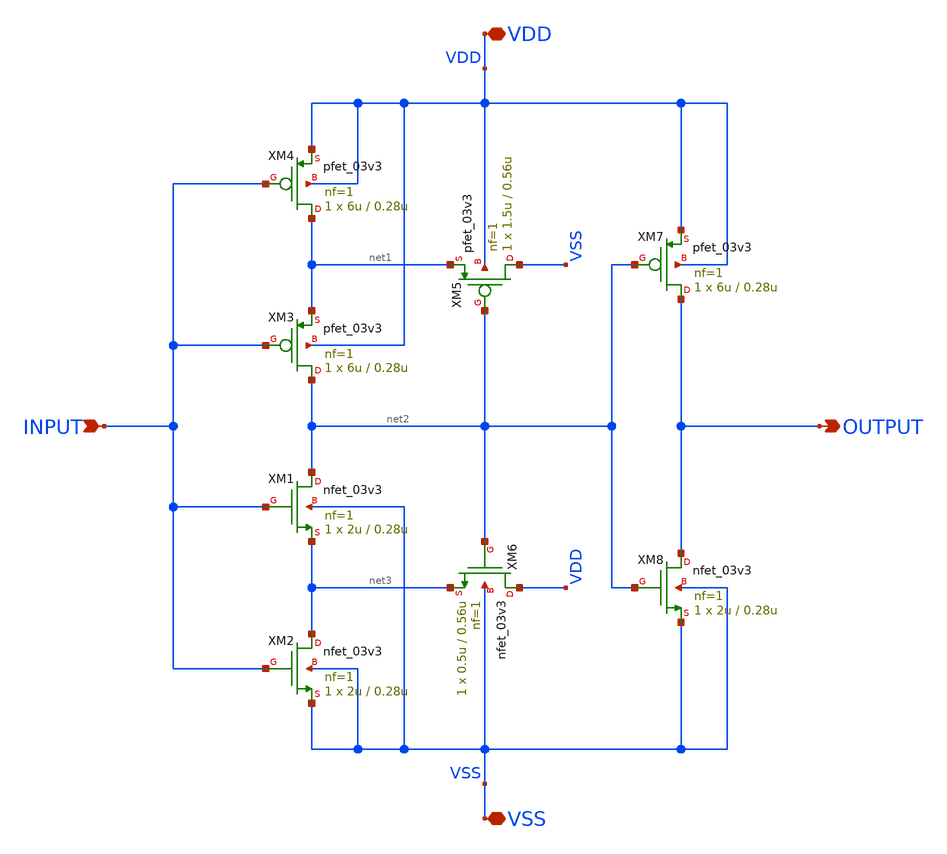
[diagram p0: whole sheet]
** sch_path: designs/schmitt_trigger/schmitt_trigger.sch
**.subckt schmitt_trigger INPUT OUTPUT VSS VDD
*.ipin INPUT
*.opin OUTPUT
*.iopin VSS
*.iopin VDD
XM1 net2 INPUT net3 VSS nfet_03v3 L=0.28u W=2u nf=1 ad='int((nf+1)/2) * W/nf * 0.18u' as='int((nf+2)/2) * W/nf * 0.18u'
+ pd='2*int((nf+1)/2) * (W/nf + 0.18u)' ps='2*int((nf+2)/2) * (W/nf + 0.18u)' nrd='0.18u / W' nrs='0.18u / W'
+ sa=0 sb=0 sd=0 m=1
XM2 net3 INPUT VSS VSS nfet_03v3 L=0.28u W=2u nf=1 ad='int((nf+1)/2) * W/nf * 0.18u' as='int((nf+2)/2) * W/nf * 0.18u'
+ pd='2*int((nf+1)/2) * (W/nf + 0.18u)' ps='2*int((nf+2)/2) * (W/nf + 0.18u)' nrd='0.18u / W' nrs='0.18u / W'
+ sa=0 sb=0 sd=0 m=1
XM3 net2 INPUT net1 VDD pfet_03v3 L=0.28u W=6u nf=1 ad='int((nf+1)/2) * W/nf * 0.18u' as='int((nf+2)/2) * W/nf * 0.18u'
+ pd='2*int((nf+1)/2) * (W/nf + 0.18u)' ps='2*int((nf+2)/2) * (W/nf + 0.18u)' nrd='0.18u / W' nrs='0.18u / W'
+ sa=0 sb=0 sd=0 m=1
XM4 net1 INPUT VDD VDD pfet_03v3 L=0.28u W=6u nf=1 ad='int((nf+1)/2) * W/nf * 0.18u' as='int((nf+2)/2) * W/nf * 0.18u'
+ pd='2*int((nf+1)/2) * (W/nf + 0.18u)' ps='2*int((nf+2)/2) * (W/nf + 0.18u)' nrd='0.18u / W' nrs='0.18u / W'
+ sa=0 sb=0 sd=0 m=1
XM5 VSS net2 net1 VDD pfet_03v3 L=0.56u W=1.5u nf=1 ad='int((nf+1)/2) * W/nf * 0.18u' as='int((nf+2)/2) * W/nf * 0.18u'
+ pd='2*int((nf+1)/2) * (W/nf + 0.18u)' ps='2*int((nf+2)/2) * (W/nf + 0.18u)' nrd='0.18u / W' nrs='0.18u / W'
+ sa=0 sb=0 sd=0 m=1
XM6 VDD net2 net3 VSS nfet_03v3 L=0.56u W=0.5u nf=1 ad='int((nf+1)/2) * W/nf * 0.18u' as='int((nf+2)/2) * W/nf * 0.18u'
+ pd='2*int((nf+1)/2) * (W/nf + 0.18u)' ps='2*int((nf+2)/2) * (W/nf + 0.18u)' nrd='0.18u / W' nrs='0.18u / W'
+ sa=0 sb=0 sd=0 m=1
XM7 OUTPUT net2 VDD VDD pfet_03v3 L=0.28u W=6u nf=1 ad='int((nf+1)/2) * W/nf * 0.18u' as='int((nf+2)/2) * W/nf * 0.18u'
+ pd='2*int((nf+1)/2) * (W/nf + 0.18u)' ps='2*int((nf+2)/2) * (W/nf + 0.18u)' nrd='0.18u / W' nrs='0.18u / W'
+ sa=0 sb=0 sd=0 m=1
XM8 OUTPUT net2 VSS VSS nfet_03v3 L=0.28u W=2u nf=1 ad='int((nf+1)/2) * W/nf * 0.18u' as='int((nf+2)/2) * W/nf * 0.18u'
+ pd='2*int((nf+1)/2) * (W/nf + 0.18u)' ps='2*int((nf+2)/2) * (W/nf + 0.18u)' nrd='0.18u / W' nrs='0.18u / W'
+ sa=0 sb=0 sd=0 m=1
**.ends
.end
